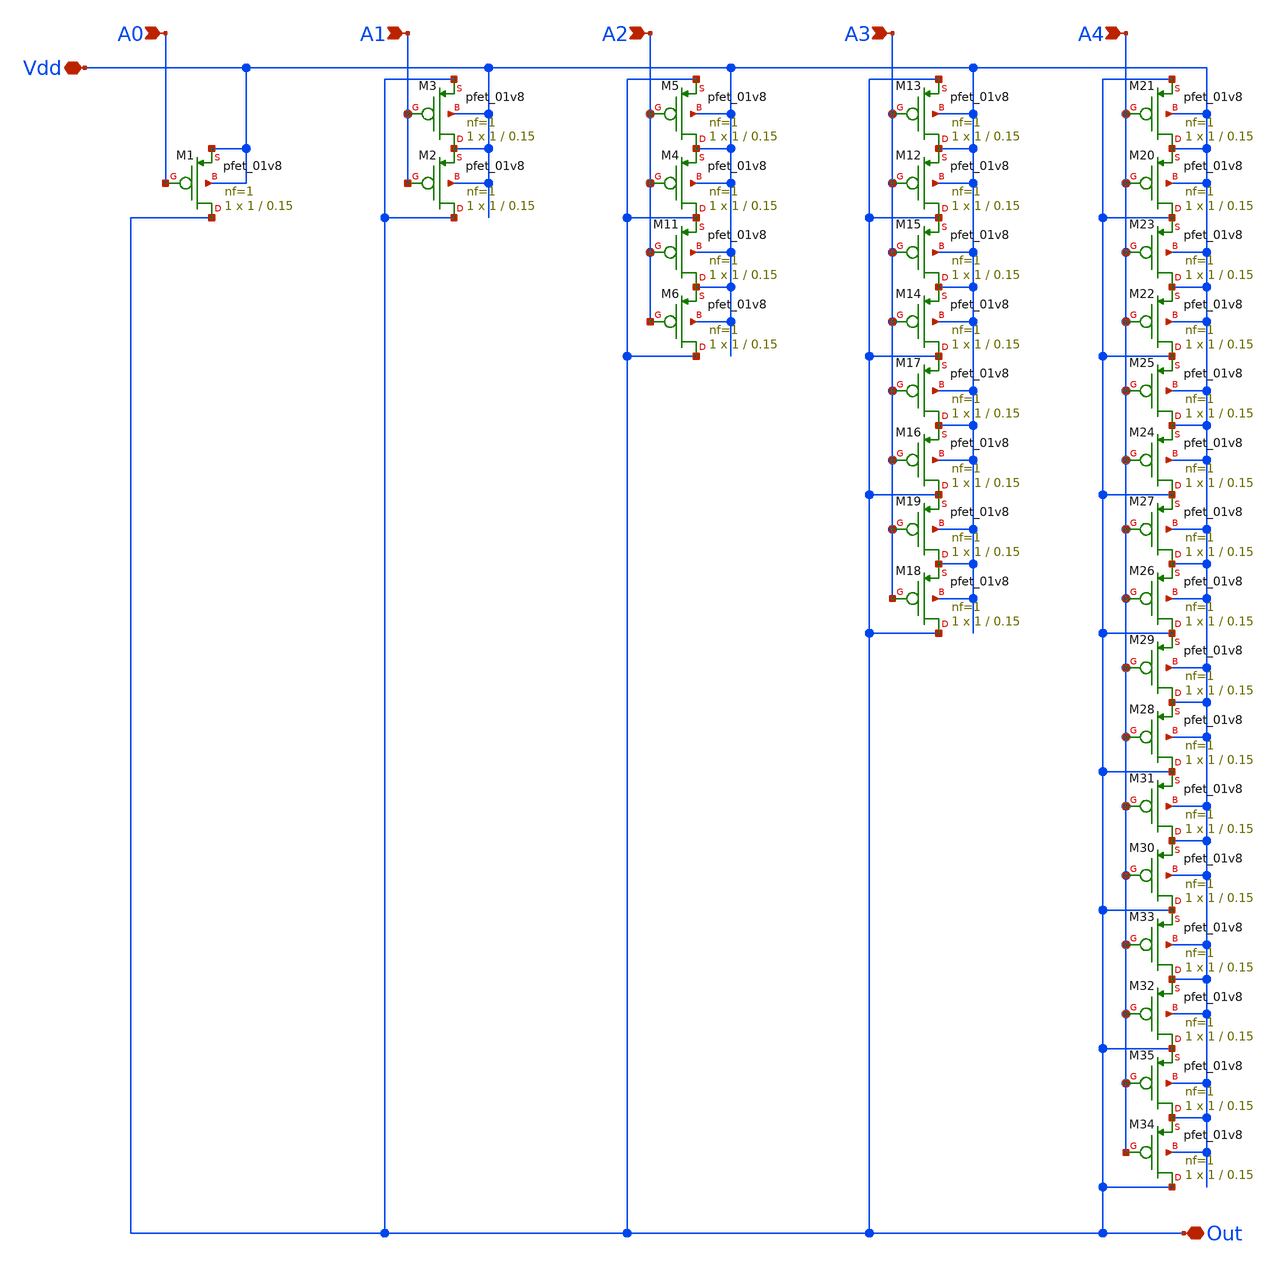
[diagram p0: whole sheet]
** sch_path: libs.ref/sky130_hilas_sc/xschem/DAC5bit01.sch
**.subckt DAC5bit01 Vdd A4 Out A3 A2 A1 A0
*.iopin Vdd
*.ipin A4
*.iopin Out
*.ipin A3
*.ipin A2
*.ipin A1
*.ipin A0
XM1 Out A0 Vdd Vdd sky130_fd_pr__pfet_01v8 L=0.15 W=1 nf=1 ad='int((nf+1)/2) * W/nf * 0.29' as='int((nf+2)/2) * W/nf * 0.29'
+ pd='2*int((nf+1)/2) * (W/nf + 0.29)' ps='2*int((nf+2)/2) * (W/nf + 0.29)' nrd='0.29 / W' nrs='0.29 / W'
+ sa=0 sb=0 sd=0 mult=1 m=1
XM2 Out A1 Vdd Vdd sky130_fd_pr__pfet_01v8 L=0.15 W=1 nf=1 ad='int((nf+1)/2) * W/nf * 0.29' as='int((nf+2)/2) * W/nf * 0.29'
+ pd='2*int((nf+1)/2) * (W/nf + 0.29)' ps='2*int((nf+2)/2) * (W/nf + 0.29)' nrd='0.29 / W' nrs='0.29 / W'
+ sa=0 sb=0 sd=0 mult=1 m=1
XM3 Vdd A1 Out Vdd sky130_fd_pr__pfet_01v8 L=0.15 W=1 nf=1 ad='int((nf+1)/2) * W/nf * 0.29' as='int((nf+2)/2) * W/nf * 0.29'
+ pd='2*int((nf+1)/2) * (W/nf + 0.29)' ps='2*int((nf+2)/2) * (W/nf + 0.29)' nrd='0.29 / W' nrs='0.29 / W'
+ sa=0 sb=0 sd=0 mult=1 m=1
XM4 Out A2 Vdd Vdd sky130_fd_pr__pfet_01v8 L=0.15 W=1 nf=1 ad='int((nf+1)/2) * W/nf * 0.29' as='int((nf+2)/2) * W/nf * 0.29'
+ pd='2*int((nf+1)/2) * (W/nf + 0.29)' ps='2*int((nf+2)/2) * (W/nf + 0.29)' nrd='0.29 / W' nrs='0.29 / W'
+ sa=0 sb=0 sd=0 mult=1 m=1
XM5 Vdd A2 Out Vdd sky130_fd_pr__pfet_01v8 L=0.15 W=1 nf=1 ad='int((nf+1)/2) * W/nf * 0.29' as='int((nf+2)/2) * W/nf * 0.29'
+ pd='2*int((nf+1)/2) * (W/nf + 0.29)' ps='2*int((nf+2)/2) * (W/nf + 0.29)' nrd='0.29 / W' nrs='0.29 / W'
+ sa=0 sb=0 sd=0 mult=1 m=1
XM6 Out A2 Vdd Vdd sky130_fd_pr__pfet_01v8 L=0.15 W=1 nf=1 ad='int((nf+1)/2) * W/nf * 0.29' as='int((nf+2)/2) * W/nf * 0.29'
+ pd='2*int((nf+1)/2) * (W/nf + 0.29)' ps='2*int((nf+2)/2) * (W/nf + 0.29)' nrd='0.29 / W' nrs='0.29 / W'
+ sa=0 sb=0 sd=0 mult=1 m=1
XM11 Vdd A2 Out Vdd sky130_fd_pr__pfet_01v8 L=0.15 W=1 nf=1 ad='int((nf+1)/2) * W/nf * 0.29' as='int((nf+2)/2) * W/nf * 0.29'
+ pd='2*int((nf+1)/2) * (W/nf + 0.29)' ps='2*int((nf+2)/2) * (W/nf + 0.29)' nrd='0.29 / W' nrs='0.29 / W'
+ sa=0 sb=0 sd=0 mult=1 m=1
XM12 Out A3 Vdd Vdd sky130_fd_pr__pfet_01v8 L=0.15 W=1 nf=1 ad='int((nf+1)/2) * W/nf * 0.29' as='int((nf+2)/2) * W/nf * 0.29'
+ pd='2*int((nf+1)/2) * (W/nf + 0.29)' ps='2*int((nf+2)/2) * (W/nf + 0.29)' nrd='0.29 / W' nrs='0.29 / W'
+ sa=0 sb=0 sd=0 mult=1 m=1
XM13 Vdd A3 Out Vdd sky130_fd_pr__pfet_01v8 L=0.15 W=1 nf=1 ad='int((nf+1)/2) * W/nf * 0.29' as='int((nf+2)/2) * W/nf * 0.29'
+ pd='2*int((nf+1)/2) * (W/nf + 0.29)' ps='2*int((nf+2)/2) * (W/nf + 0.29)' nrd='0.29 / W' nrs='0.29 / W'
+ sa=0 sb=0 sd=0 mult=1 m=1
XM14 Out A3 Vdd Vdd sky130_fd_pr__pfet_01v8 L=0.15 W=1 nf=1 ad='int((nf+1)/2) * W/nf * 0.29' as='int((nf+2)/2) * W/nf * 0.29'
+ pd='2*int((nf+1)/2) * (W/nf + 0.29)' ps='2*int((nf+2)/2) * (W/nf + 0.29)' nrd='0.29 / W' nrs='0.29 / W'
+ sa=0 sb=0 sd=0 mult=1 m=1
XM15 Vdd A3 Out Vdd sky130_fd_pr__pfet_01v8 L=0.15 W=1 nf=1 ad='int((nf+1)/2) * W/nf * 0.29' as='int((nf+2)/2) * W/nf * 0.29'
+ pd='2*int((nf+1)/2) * (W/nf + 0.29)' ps='2*int((nf+2)/2) * (W/nf + 0.29)' nrd='0.29 / W' nrs='0.29 / W'
+ sa=0 sb=0 sd=0 mult=1 m=1
XM16 Out A3 Vdd Vdd sky130_fd_pr__pfet_01v8 L=0.15 W=1 nf=1 ad='int((nf+1)/2) * W/nf * 0.29' as='int((nf+2)/2) * W/nf * 0.29'
+ pd='2*int((nf+1)/2) * (W/nf + 0.29)' ps='2*int((nf+2)/2) * (W/nf + 0.29)' nrd='0.29 / W' nrs='0.29 / W'
+ sa=0 sb=0 sd=0 mult=1 m=1
XM17 Vdd A3 Out Vdd sky130_fd_pr__pfet_01v8 L=0.15 W=1 nf=1 ad='int((nf+1)/2) * W/nf * 0.29' as='int((nf+2)/2) * W/nf * 0.29'
+ pd='2*int((nf+1)/2) * (W/nf + 0.29)' ps='2*int((nf+2)/2) * (W/nf + 0.29)' nrd='0.29 / W' nrs='0.29 / W'
+ sa=0 sb=0 sd=0 mult=1 m=1
XM18 Out A3 Vdd Vdd sky130_fd_pr__pfet_01v8 L=0.15 W=1 nf=1 ad='int((nf+1)/2) * W/nf * 0.29' as='int((nf+2)/2) * W/nf * 0.29'
+ pd='2*int((nf+1)/2) * (W/nf + 0.29)' ps='2*int((nf+2)/2) * (W/nf + 0.29)' nrd='0.29 / W' nrs='0.29 / W'
+ sa=0 sb=0 sd=0 mult=1 m=1
XM19 Vdd A3 Out Vdd sky130_fd_pr__pfet_01v8 L=0.15 W=1 nf=1 ad='int((nf+1)/2) * W/nf * 0.29' as='int((nf+2)/2) * W/nf * 0.29'
+ pd='2*int((nf+1)/2) * (W/nf + 0.29)' ps='2*int((nf+2)/2) * (W/nf + 0.29)' nrd='0.29 / W' nrs='0.29 / W'
+ sa=0 sb=0 sd=0 mult=1 m=1
XM20 Out A4 Vdd Vdd sky130_fd_pr__pfet_01v8 L=0.15 W=1 nf=1 ad='int((nf+1)/2) * W/nf * 0.29' as='int((nf+2)/2) * W/nf * 0.29'
+ pd='2*int((nf+1)/2) * (W/nf + 0.29)' ps='2*int((nf+2)/2) * (W/nf + 0.29)' nrd='0.29 / W' nrs='0.29 / W'
+ sa=0 sb=0 sd=0 mult=1 m=1
XM21 Vdd A4 Out Vdd sky130_fd_pr__pfet_01v8 L=0.15 W=1 nf=1 ad='int((nf+1)/2) * W/nf * 0.29' as='int((nf+2)/2) * W/nf * 0.29'
+ pd='2*int((nf+1)/2) * (W/nf + 0.29)' ps='2*int((nf+2)/2) * (W/nf + 0.29)' nrd='0.29 / W' nrs='0.29 / W'
+ sa=0 sb=0 sd=0 mult=1 m=1
XM22 Out A4 Vdd Vdd sky130_fd_pr__pfet_01v8 L=0.15 W=1 nf=1 ad='int((nf+1)/2) * W/nf * 0.29' as='int((nf+2)/2) * W/nf * 0.29'
+ pd='2*int((nf+1)/2) * (W/nf + 0.29)' ps='2*int((nf+2)/2) * (W/nf + 0.29)' nrd='0.29 / W' nrs='0.29 / W'
+ sa=0 sb=0 sd=0 mult=1 m=1
XM23 Vdd A4 Out Vdd sky130_fd_pr__pfet_01v8 L=0.15 W=1 nf=1 ad='int((nf+1)/2) * W/nf * 0.29' as='int((nf+2)/2) * W/nf * 0.29'
+ pd='2*int((nf+1)/2) * (W/nf + 0.29)' ps='2*int((nf+2)/2) * (W/nf + 0.29)' nrd='0.29 / W' nrs='0.29 / W'
+ sa=0 sb=0 sd=0 mult=1 m=1
XM24 Out A4 Vdd Vdd sky130_fd_pr__pfet_01v8 L=0.15 W=1 nf=1 ad='int((nf+1)/2) * W/nf * 0.29' as='int((nf+2)/2) * W/nf * 0.29'
+ pd='2*int((nf+1)/2) * (W/nf + 0.29)' ps='2*int((nf+2)/2) * (W/nf + 0.29)' nrd='0.29 / W' nrs='0.29 / W'
+ sa=0 sb=0 sd=0 mult=1 m=1
XM25 Vdd A4 Out Vdd sky130_fd_pr__pfet_01v8 L=0.15 W=1 nf=1 ad='int((nf+1)/2) * W/nf * 0.29' as='int((nf+2)/2) * W/nf * 0.29'
+ pd='2*int((nf+1)/2) * (W/nf + 0.29)' ps='2*int((nf+2)/2) * (W/nf + 0.29)' nrd='0.29 / W' nrs='0.29 / W'
+ sa=0 sb=0 sd=0 mult=1 m=1
XM26 Out A4 Vdd Vdd sky130_fd_pr__pfet_01v8 L=0.15 W=1 nf=1 ad='int((nf+1)/2) * W/nf * 0.29' as='int((nf+2)/2) * W/nf * 0.29'
+ pd='2*int((nf+1)/2) * (W/nf + 0.29)' ps='2*int((nf+2)/2) * (W/nf + 0.29)' nrd='0.29 / W' nrs='0.29 / W'
+ sa=0 sb=0 sd=0 mult=1 m=1
XM27 Vdd A4 Out Vdd sky130_fd_pr__pfet_01v8 L=0.15 W=1 nf=1 ad='int((nf+1)/2) * W/nf * 0.29' as='int((nf+2)/2) * W/nf * 0.29'
+ pd='2*int((nf+1)/2) * (W/nf + 0.29)' ps='2*int((nf+2)/2) * (W/nf + 0.29)' nrd='0.29 / W' nrs='0.29 / W'
+ sa=0 sb=0 sd=0 mult=1 m=1
XM28 Out A4 Vdd Vdd sky130_fd_pr__pfet_01v8 L=0.15 W=1 nf=1 ad='int((nf+1)/2) * W/nf * 0.29' as='int((nf+2)/2) * W/nf * 0.29'
+ pd='2*int((nf+1)/2) * (W/nf + 0.29)' ps='2*int((nf+2)/2) * (W/nf + 0.29)' nrd='0.29 / W' nrs='0.29 / W'
+ sa=0 sb=0 sd=0 mult=1 m=1
XM29 Vdd A4 Out Vdd sky130_fd_pr__pfet_01v8 L=0.15 W=1 nf=1 ad='int((nf+1)/2) * W/nf * 0.29' as='int((nf+2)/2) * W/nf * 0.29'
+ pd='2*int((nf+1)/2) * (W/nf + 0.29)' ps='2*int((nf+2)/2) * (W/nf + 0.29)' nrd='0.29 / W' nrs='0.29 / W'
+ sa=0 sb=0 sd=0 mult=1 m=1
XM30 Out A4 Vdd Vdd sky130_fd_pr__pfet_01v8 L=0.15 W=1 nf=1 ad='int((nf+1)/2) * W/nf * 0.29' as='int((nf+2)/2) * W/nf * 0.29'
+ pd='2*int((nf+1)/2) * (W/nf + 0.29)' ps='2*int((nf+2)/2) * (W/nf + 0.29)' nrd='0.29 / W' nrs='0.29 / W'
+ sa=0 sb=0 sd=0 mult=1 m=1
XM31 Vdd A4 Out Vdd sky130_fd_pr__pfet_01v8 L=0.15 W=1 nf=1 ad='int((nf+1)/2) * W/nf * 0.29' as='int((nf+2)/2) * W/nf * 0.29'
+ pd='2*int((nf+1)/2) * (W/nf + 0.29)' ps='2*int((nf+2)/2) * (W/nf + 0.29)' nrd='0.29 / W' nrs='0.29 / W'
+ sa=0 sb=0 sd=0 mult=1 m=1
XM32 Out A4 Vdd Vdd sky130_fd_pr__pfet_01v8 L=0.15 W=1 nf=1 ad='int((nf+1)/2) * W/nf * 0.29' as='int((nf+2)/2) * W/nf * 0.29'
+ pd='2*int((nf+1)/2) * (W/nf + 0.29)' ps='2*int((nf+2)/2) * (W/nf + 0.29)' nrd='0.29 / W' nrs='0.29 / W'
+ sa=0 sb=0 sd=0 mult=1 m=1
XM33 Vdd A4 Out Vdd sky130_fd_pr__pfet_01v8 L=0.15 W=1 nf=1 ad='int((nf+1)/2) * W/nf * 0.29' as='int((nf+2)/2) * W/nf * 0.29'
+ pd='2*int((nf+1)/2) * (W/nf + 0.29)' ps='2*int((nf+2)/2) * (W/nf + 0.29)' nrd='0.29 / W' nrs='0.29 / W'
+ sa=0 sb=0 sd=0 mult=1 m=1
XM34 Out A4 Vdd Vdd sky130_fd_pr__pfet_01v8 L=0.15 W=1 nf=1 ad='int((nf+1)/2) * W/nf * 0.29' as='int((nf+2)/2) * W/nf * 0.29'
+ pd='2*int((nf+1)/2) * (W/nf + 0.29)' ps='2*int((nf+2)/2) * (W/nf + 0.29)' nrd='0.29 / W' nrs='0.29 / W'
+ sa=0 sb=0 sd=0 mult=1 m=1
XM35 Vdd A4 Out Vdd sky130_fd_pr__pfet_01v8 L=0.15 W=1 nf=1 ad='int((nf+1)/2) * W/nf * 0.29' as='int((nf+2)/2) * W/nf * 0.29'
+ pd='2*int((nf+1)/2) * (W/nf + 0.29)' ps='2*int((nf+2)/2) * (W/nf + 0.29)' nrd='0.29 / W' nrs='0.29 / W'
+ sa=0 sb=0 sd=0 mult=1 m=1
**.ends
.end
